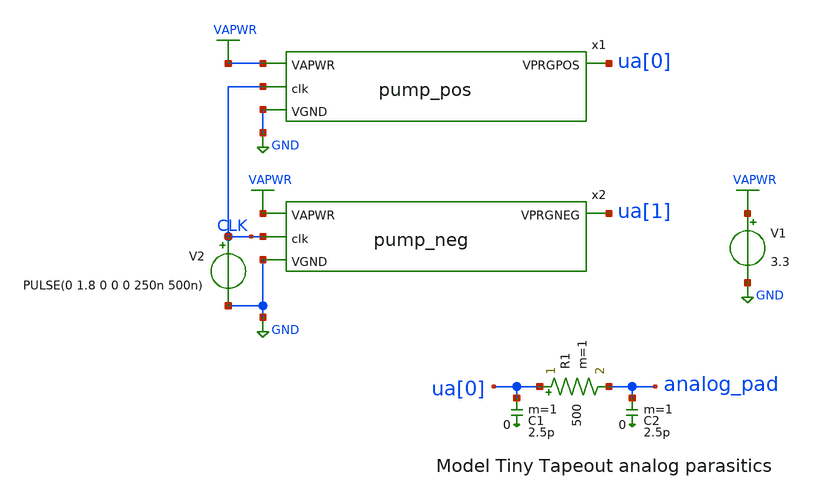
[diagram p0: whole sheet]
** sch_path: xschem/testbench.sch
**.subckt testbench
V1 VAPWR GND 3.3
V2 CLK GND PULSE(0 1.8 0 0 0 250n 500n)
R1 ua[0] analog_pad 500 m=1
C1 ua[0] 0 2.5p m=1
C2 analog_pad 0 2.5p m=1
x1 VAPWR ua[0] CLK GND pump_pos
x2 VAPWR ua[1] CLK GND pump_neg
**** begin user architecture code

** opencircuitdesign pdks install
.lib $::SKYWATER_MODELS/sky130.lib.spice tt





.tran 10n 100u
.save all

.control
run
write testbench.raw
.endc


**** end user architecture code
**.ends
.GLOBAL GND
.GLOBAL VAPWR
.end
